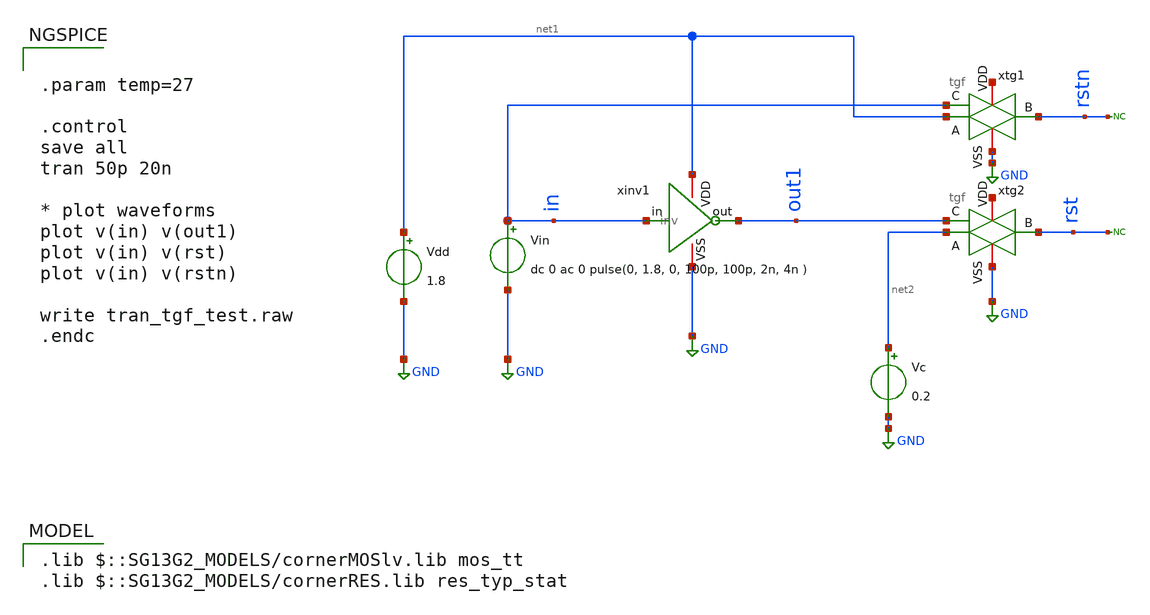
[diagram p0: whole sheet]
** sch_path: blocks/composite/dpi_adexp_neuron/design_data/xschem/switch_tb.sch
**.subckt switch_tb
xtg1 net3 in net1 rstn GND tgf
Vdd net1 GND 1.8
Vin in GND dc 0 ac 0 pulse(0, 1.8, 0, 100p, 100p, 2n, 4n )
* noconn rstn
xinv1 net1 in out1 GND inv
xtg2 net4 out1 net2 rst GND tgf
Vc net2 GND 0.2
* noconn rst
**** begin user architecture code


.param temp=27

.control
save all
tran 50p 20n

* plot waveforms
plot v(in) v(out1)
plot v(in) v(rst)
plot v(in) v(rstn)

write tran_tgf_test.raw
.endc



 .lib $::SG13G2_MODELS/cornerMOSlv.lib mos_tt
.lib $::SG13G2_MODELS/cornerRES.lib res_typ_stat

**** end user architecture code
**.ends
.GLOBAL GND
.end
